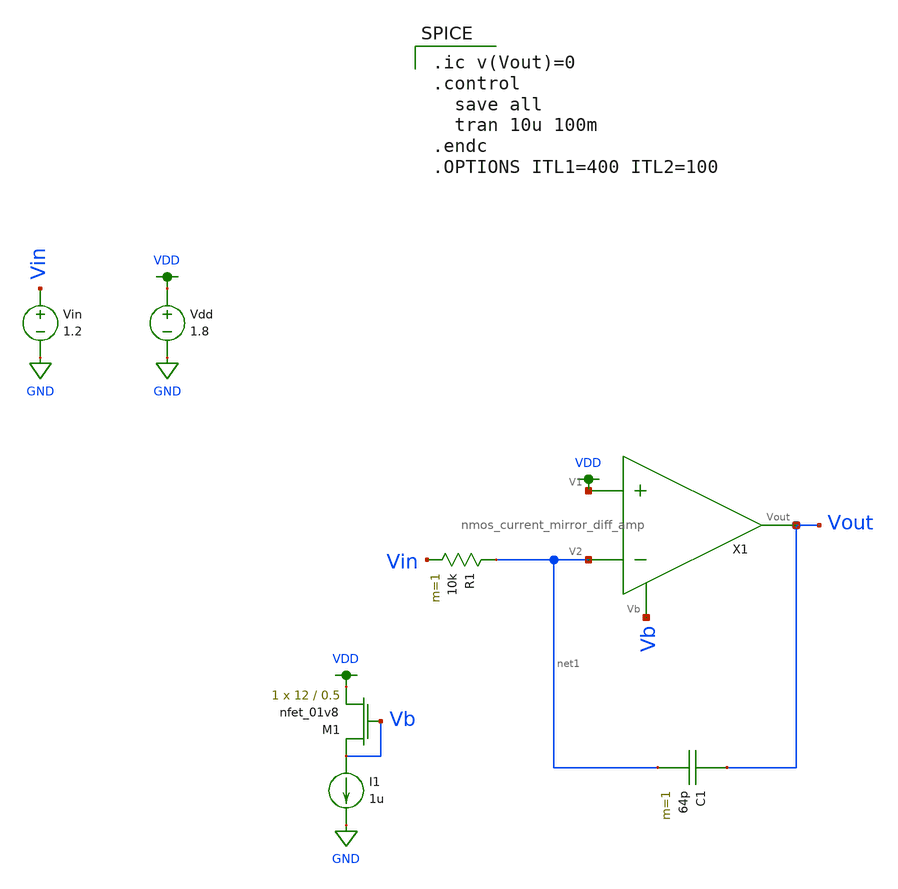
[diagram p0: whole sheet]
** sch_path: schematic/nmos_integrator_test.sch
**.subckt nmos_integrator_test
Vdd VDD GND 1.8
Vin Vin GND 1.2
C1 Vout net1 64p m=1
I1 Vb GND 1u
R1 net1 Vin 10k m=1
X1 Vb Vout VDD net1 nmos_current_mirror_diff_amp
XM1 Vb Vb VDD GND sky130_fd_pr__nfet_01v8 L=0.5 W=12 nf=1 ad='int((nf+1)/2) * W/nf * 0.29' as='int((nf+2)/2) * W/nf * 0.29'
+ pd='2*int((nf+1)/2) * (W/nf + 0.29)' ps='2*int((nf+2)/2) * (W/nf + 0.29)' nrd='0.29 / W' nrs='0.29 / W'
+ sa=0 sb=0 sd=0 mult=1 m=1
**** begin user architecture code

.ic v(Vout)=0
.control
  save all
  tran 10u 100m
.endc
.OPTIONS ITL1=400 ITL2=100


.option wnflag=1
.param MC_SWITCH=0.0
.lib ~/skywater/skywater-pdk/libraries/sky130_fd_pr_ngspice/latest/models/sky130.lib.spice tt

**** end user architecture code
**.ends

* expanding   symbol:
*+  /home/madvlsi/Documents/MADVLSI-Final_Project/schematic/nmos_current_mirror_diff_amp.sym # of pins=4
** sym_path: schematic/archive/nmos_current_mirror_diff_amp.sym
** sch_path: schematic/archive/nmos_current_mirror_diff_amp.sch
.subckt nmos_current_mirror_diff_amp Vb Vout V1 V2
*.ipin V1
*.ipin V2
*.ipin Vb
*.iopin Vout
XM1 net1 V1 net2 GND sky130_fd_pr__nfet_01v8 L=0.5 W=12 nf=1 ad='int((nf+1)/2) * W/nf * 0.29' as='int((nf+2)/2) * W/nf * 0.29'
+ pd='2*int((nf+1)/2) * (W/nf + 0.29)' ps='2*int((nf+2)/2) * (W/nf + 0.29)' nrd='0.29 / W' nrs='0.29 / W'
+ sa=0 sb=0 sd=0 mult=1 m=1
XM2 net2 V2 net3 GND sky130_fd_pr__nfet_01v8 L=0.5 W=12 nf=1 ad='int((nf+1)/2) * W/nf * 0.29' as='int((nf+2)/2) * W/nf * 0.29'
+ pd='2*int((nf+1)/2) * (W/nf + 0.29)' ps='2*int((nf+2)/2) * (W/nf + 0.29)' nrd='0.29 / W' nrs='0.29 / W'
+ sa=0 sb=0 sd=0 mult=1 m=1
XM3 net2 Vb GND GND sky130_fd_pr__nfet_01v8 L=0.5 W=12 nf=1 ad='int((nf+1)/2) * W/nf * 0.29' as='int((nf+2)/2) * W/nf * 0.29'
+ pd='2*int((nf+1)/2) * (W/nf + 0.29)' ps='2*int((nf+2)/2) * (W/nf + 0.29)' nrd='0.29 / W' nrs='0.29 / W'
+ sa=0 sb=0 sd=0 mult=1 m=1
XM4 GND net4 net4 GND sky130_fd_pr__nfet_01v8 L=0.5 W=12 nf=1 ad='int((nf+1)/2) * W/nf * 0.29' as='int((nf+2)/2) * W/nf * 0.29'
+ pd='2*int((nf+1)/2) * (W/nf + 0.29)' ps='2*int((nf+2)/2) * (W/nf + 0.29)' nrd='0.29 / W' nrs='0.29 / W'
+ sa=0 sb=0 sd=0 mult=1 m=1
XM5 Vout net4 GND GND sky130_fd_pr__nfet_01v8 L=0.5 W=12 nf=1 ad='int((nf+1)/2) * W/nf * 0.29' as='int((nf+2)/2) * W/nf * 0.29'
+ pd='2*int((nf+1)/2) * (W/nf + 0.29)' ps='2*int((nf+2)/2) * (W/nf + 0.29)' nrd='0.29 / W' nrs='0.29 / W'
+ sa=0 sb=0 sd=0 mult=1 m=1
XM6 VDD net1 net1 VDD sky130_fd_pr__pfet_01v8 L=0.5 W=12 nf=1 ad='int((nf+1)/2) * W/nf * 0.29' as='int((nf+2)/2) * W/nf * 0.29'
+ pd='2*int((nf+1)/2) * (W/nf + 0.29)' ps='2*int((nf+2)/2) * (W/nf + 0.29)' nrd='0.29 / W' nrs='0.29 / W'
+ sa=0 sb=0 sd=0 mult=1 m=1
XM7 VDD net3 net3 VDD sky130_fd_pr__pfet_01v8 L=0.5 W=12 nf=1 ad='int((nf+1)/2) * W/nf * 0.29' as='int((nf+2)/2) * W/nf * 0.29'
+ pd='2*int((nf+1)/2) * (W/nf + 0.29)' ps='2*int((nf+2)/2) * (W/nf + 0.29)' nrd='0.29 / W' nrs='0.29 / W'
+ sa=0 sb=0 sd=0 mult=1 m=1
XM8 net4 net3 VDD VDD sky130_fd_pr__pfet_01v8 L=0.5 W=12 nf=1 ad='int((nf+1)/2) * W/nf * 0.29' as='int((nf+2)/2) * W/nf * 0.29'
+ pd='2*int((nf+1)/2) * (W/nf + 0.29)' ps='2*int((nf+2)/2) * (W/nf + 0.29)' nrd='0.29 / W' nrs='0.29 / W'
+ sa=0 sb=0 sd=0 mult=1 m=1
XM9 Vout net1 VDD VDD sky130_fd_pr__pfet_01v8 L=0.5 W=12 nf=1 ad='int((nf+1)/2) * W/nf * 0.29' as='int((nf+2)/2) * W/nf * 0.29'
+ pd='2*int((nf+1)/2) * (W/nf + 0.29)' ps='2*int((nf+2)/2) * (W/nf + 0.29)' nrd='0.29 / W' nrs='0.29 / W'
+ sa=0 sb=0 sd=0 mult=1 m=1
.ends

.GLOBAL GND
.GLOBAL VDD
.end
